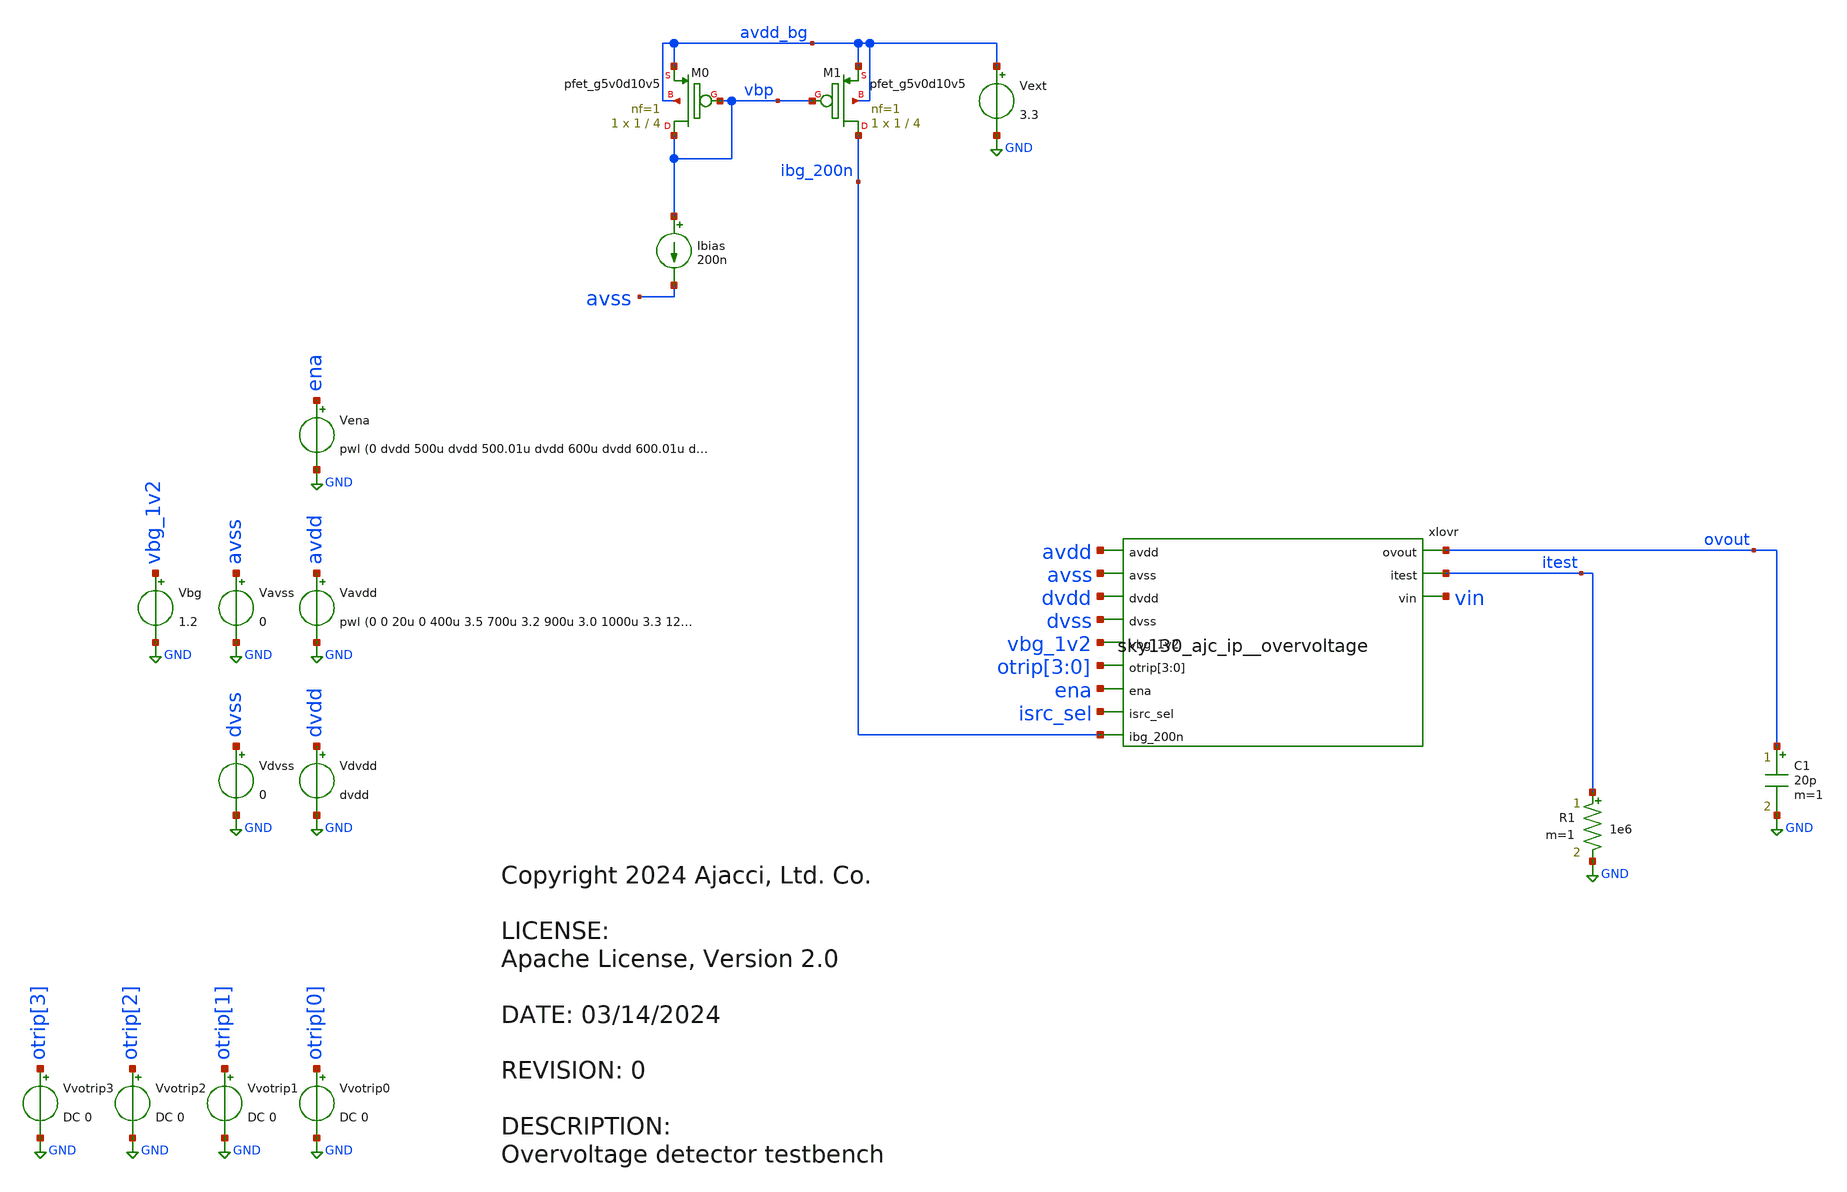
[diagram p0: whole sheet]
** sch_path: xschem/sky130_ajc_ip__overvoltage_tb.sch
* Copyright 2024 Ajacci, Ltd. Co.
* LICENSE:
* Apache License, Version 2.0
**.subckt sky130_ajc_ip__overvoltage_tb
Vavss avss GND 0
Vena ena GND pwl (0 dvdd 500u dvdd 500.01u dvdd 600u dvdd 600.01u dvdd) DC dvdd
Vavdd avdd GND pwl (0 0 20u 0 400u 3.5 700u 3.2 900u 3.0 1000u 3.3 1200u 3.5) DC avdd
.save i(vavdd)
Vbg vbg_1v2 GND 1.2
Ibias vbp avss 200n
XM1 ibg_200n vbp avdd_bg avdd_bg sky130_fd_pr__pfet_g5v0d10v5 L=4 W=1 nf=1 ad='int((nf+1)/2) * W/nf * 0.29'
+ as='int((nf+2)/2) * W/nf * 0.29' pd='2*int((nf+1)/2) * (W/nf + 0.29)' ps='2*int((nf+2)/2) * (W/nf + 0.29)'
+ nrd='0.29 / W' nrs='0.29 / W' sa=0 sb=0 sd=0 mult=1 m=1
XM0 vbp vbp avdd_bg avdd_bg sky130_fd_pr__pfet_g5v0d10v5 L=4 W=1 nf=1 ad='int((nf+1)/2) * W/nf * 0.29'
+ as='int((nf+2)/2) * W/nf * 0.29' pd='2*int((nf+1)/2) * (W/nf + 0.29)' ps='2*int((nf+2)/2) * (W/nf + 0.29)'
+ nrd='0.29 / W' nrs='0.29 / W' sa=0 sb=0 sd=0 mult=1 m=1
Vdvss dvss GND 0
Vdvdd dvdd GND dvdd
.save i(vdvdd)
R1 itest GND 1e6 m=1
C1 ovout GND 20p m=1
xIovr avdd avss dvdd dvss vbg_1v2 ovout itest otrip[3] otrip[2] otrip[1] otrip[0] vin ena isrc_sel
+ ibg_200n sky130_ajc_ip__overvoltage
Vvotrip0 otrip[0] GND DC 0
.save i(vvotrip0)
Vvotrip1 otrip[1] GND DC 0
.save i(vvotrip1)
Vvotrip2 otrip[2] GND DC 0
.save i(vvotrip2)
Vvotrip3 otrip[3] GND DC 0
.save i(vvotrip3)
Vext avdd_bg GND 3.3
.save i(vext)
**** begin user architecture code


.param avdd=3.36
.param dvdd=1.8

.lib libs.tech/ngspice/sky130.lib.spice tt
.include libs.ref/sky130_fd_sc_hvl/spice/sky130_fd_sc_hvl.spice
.include libs.ref/sky130_fd_sc_hd/spice/sky130_fd_sc_hd.spice

*dig pull up/down to set test bits
R000 ena dvdd 1e9
R001 isrc_sel dvss 1e9

.temp 25
.save all
.save @m.xiovr.xiana.xirsmux.xmena.msky130_fd_pr__nfet_g5v0d10v5[id]

.control
op
print ovout vin
*tran 10u 1400u
*plot ovout itest avdd ena vbg_1v2 vin xiovr.xiana.dcomp xiovr.xiana.dcomp_filt
*plot i(Vavdd) i(Vdvdd)
*plot @m.xiovr.xiana.xirsmux.xmena.msky130_fd_pr__nfet_g5v0d10v5[id]
*plot ovout avdd ena*0.5
.endc


**** end user architecture code
**.ends
.GLOBAL GND
.end
